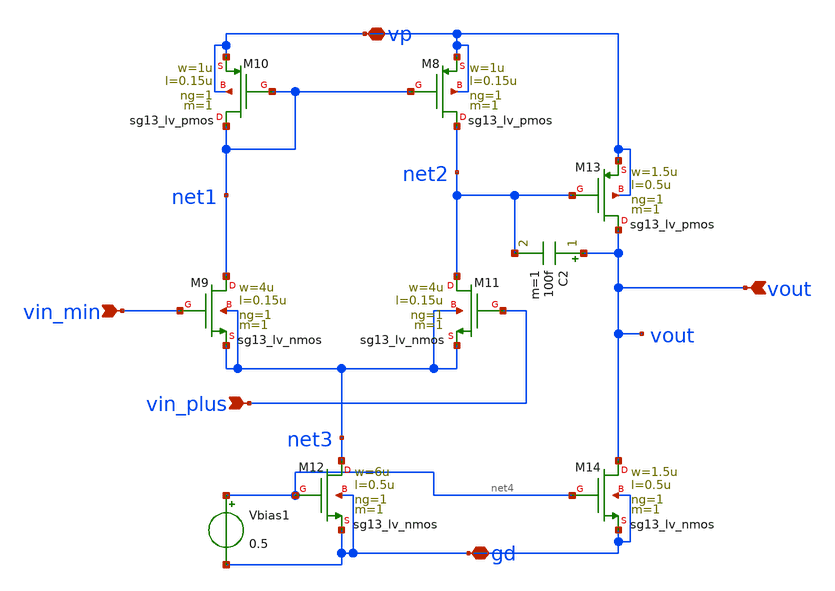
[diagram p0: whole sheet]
** sch_path: charge_pump/old_sch/amp_jj.sch
**.subckt amp_jj vp vout gd vin_min vin_plus
*.iopin vp
*.ipin vout
*.iopin gd
*.ipin vin_min
*.ipin vin_plus
XM8 net2 net1 vp vp sg13_lv_pmos w=1u l=0.15u ng=1 m=1 mm_ok=1
XM9 net1 vin_min net3 net3 sg13_lv_nmos w=4u l=0.15u ng=1 m=1 mm_ok=1
XM10 net1 net1 vp vp sg13_lv_pmos w=1u l=0.15u ng=1 m=1 mm_ok=1
XM11 net2 vin_plus net3 net3 sg13_lv_nmos w=4u l=0.15u ng=1 m=1 mm_ok=1
XM12 net3 net4 gd gd sg13_lv_nmos w=6u l=0.5u ng=1 m=1 mm_ok=1
XM13 vout net2 vp vp sg13_lv_pmos w=1.5u l=0.5u ng=1 m=1 mm_ok=1
XM14 vout net4 gd gd sg13_lv_nmos w=1.5u l=0.5u ng=1 m=1 mm_ok=1
Vbias1 net4 gd 0.5
C2 vout net2 100f m=1
**.ends
.end
